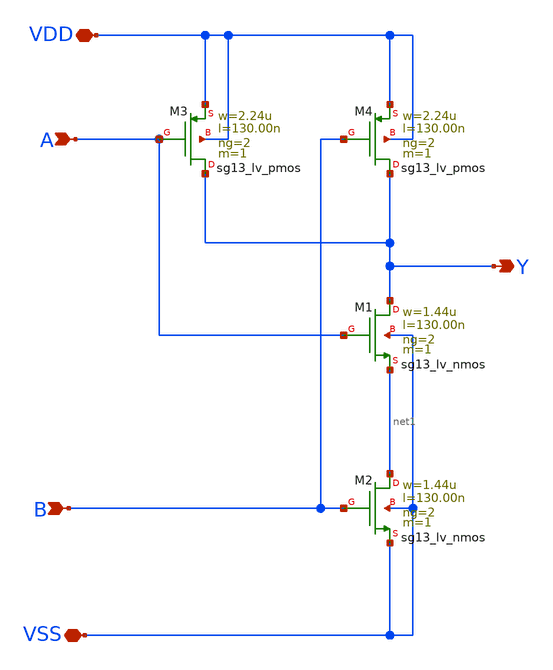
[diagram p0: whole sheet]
** sch_path: ihp-sg13g2/libs.tech/xschem/sg13g2_stdcells/sg13g2_nand2_2.sch
**.subckt sg13g2_nand2_2 VDD VSS Y B A
*.iopin VDD
*.iopin VSS
*.opin Y
*.ipin B
*.ipin A
XM1 Y A net1 VSS sg13_lv_nmos w=1.44u l=130.00n ng=2 m=1 mm_ok=1
XM2 net1 B VSS VSS sg13_lv_nmos w=1.44u l=130.00n ng=2 m=1 mm_ok=1
XM3 Y A VDD VDD sg13_lv_pmos w=2.24u l=130.00n ng=2 m=1 mm_ok=1
XM4 Y B VDD VDD sg13_lv_pmos w=2.24u l=130.00n ng=2 m=1 mm_ok=1
**.ends
.end
